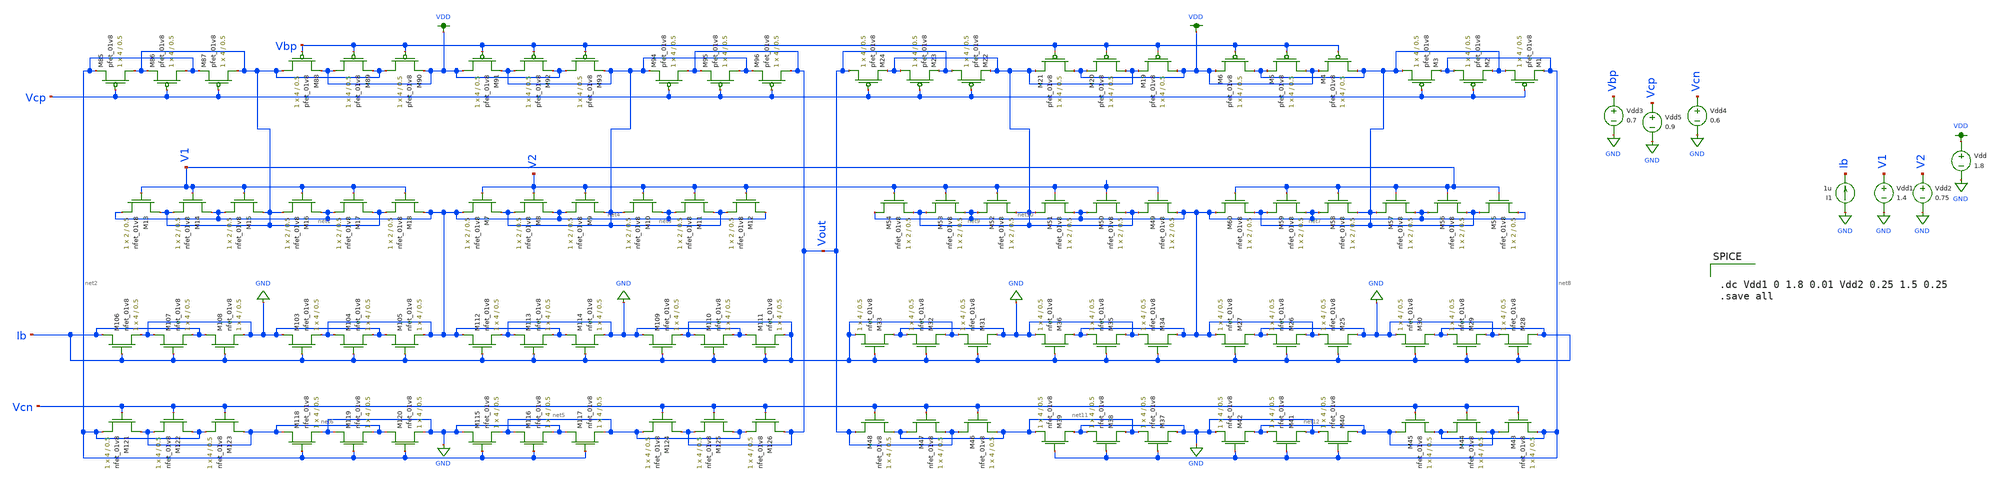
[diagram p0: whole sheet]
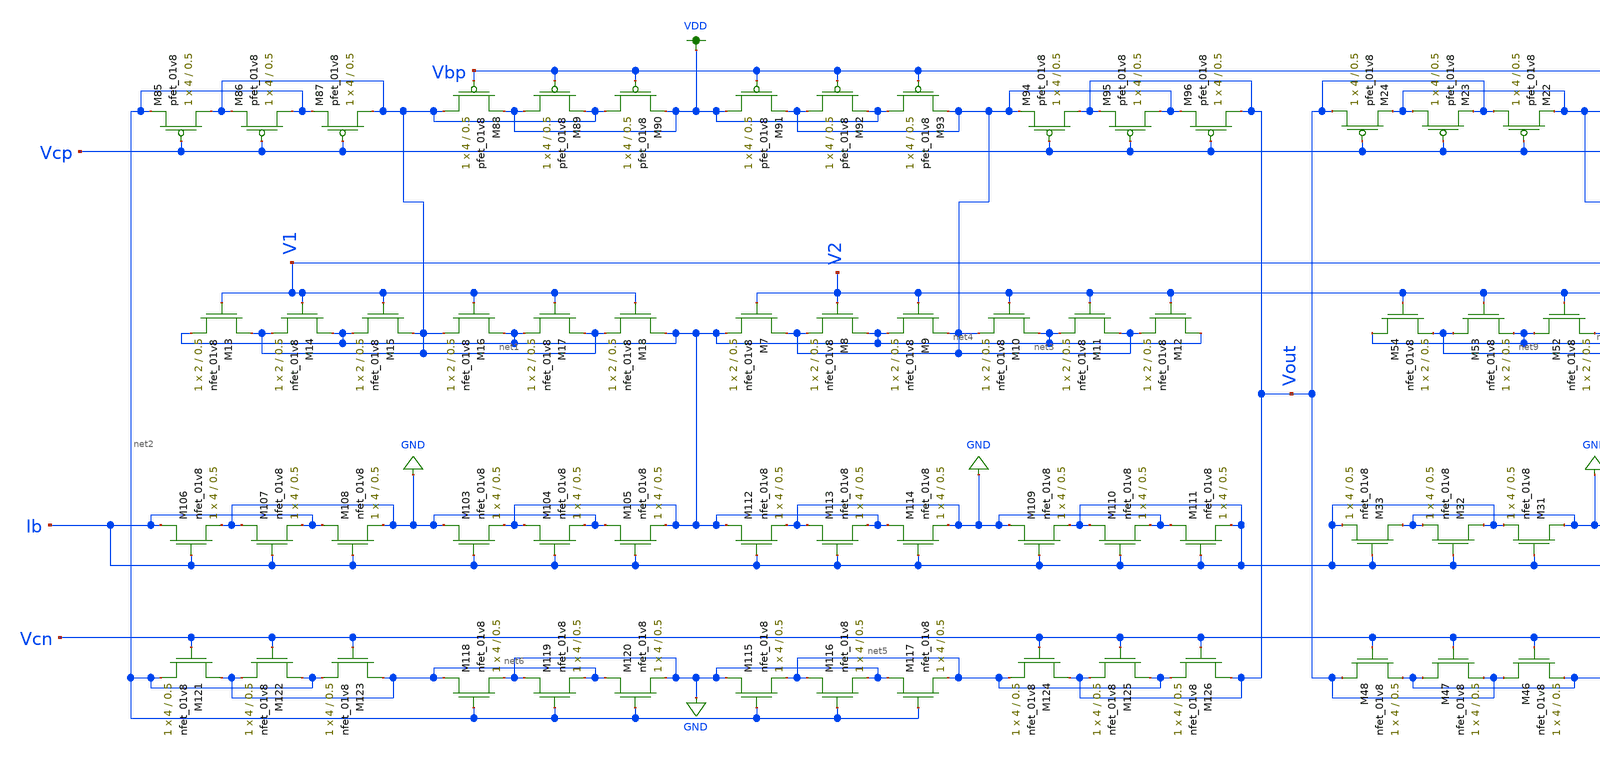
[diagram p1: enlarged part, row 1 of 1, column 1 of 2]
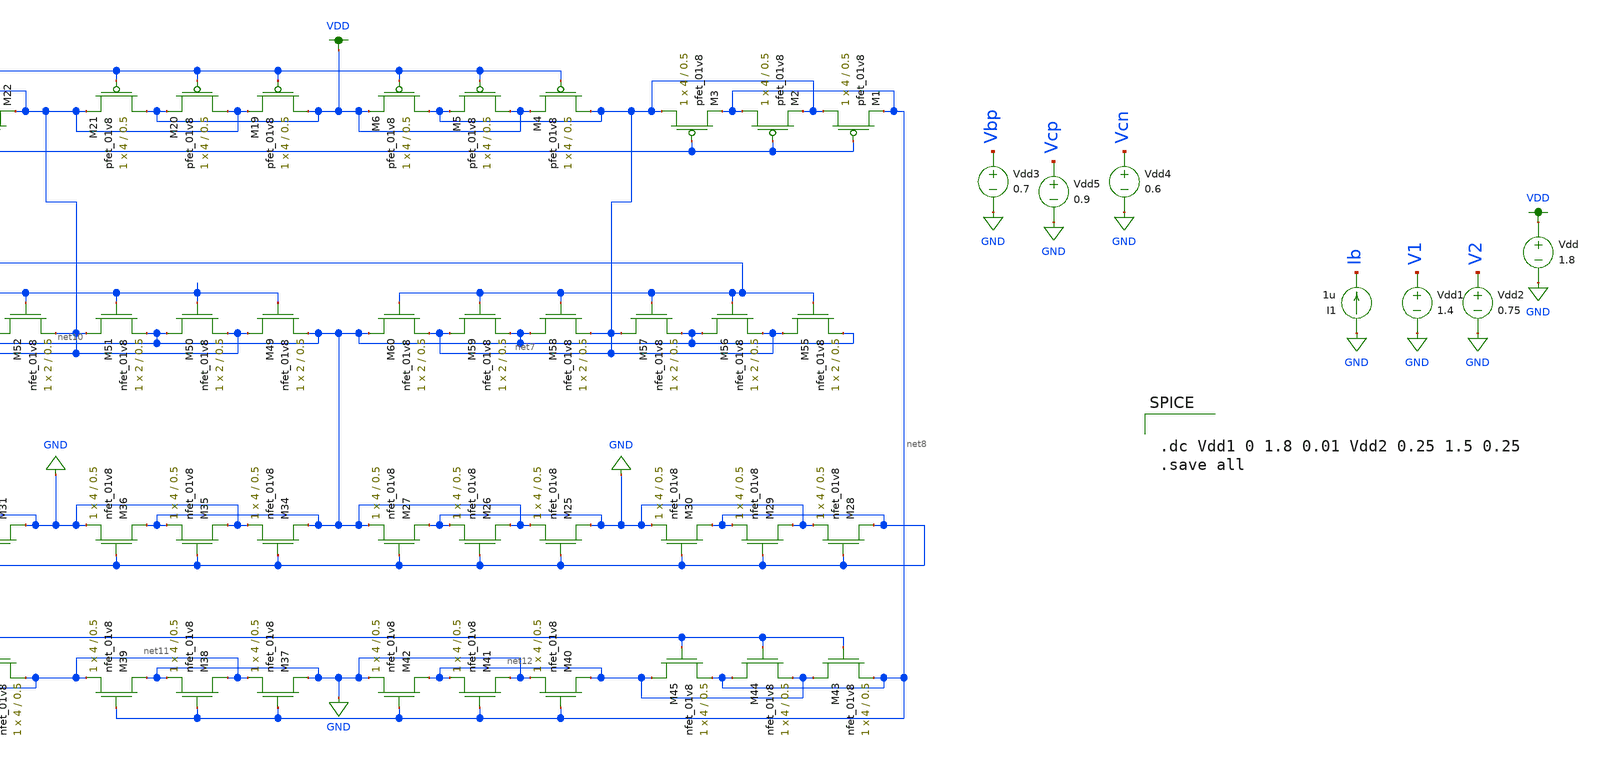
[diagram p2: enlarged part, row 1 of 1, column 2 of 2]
** sch_path: mp3/schematic/amp_lds_tran.sch
**.subckt amp_lds_tran
Vdd1 V1 GND 1.4
Vdd2 V2 GND 0.75
I1 GND Ib 1u
Vdd VDD GND 1.8
XM85 net1 Vcp net2 VDD sky130_fd_pr__pfet_01v8 L=0.5 W=4 nf=1 ad='int((nf+1)/2) * W/nf * 0.29' as='int((nf+2)/2) * W/nf * 0.29'
+ pd='2*int((nf+1)/2) * (W/nf + 0.29)' ps='2*int((nf+2)/2) * (W/nf + 0.29)' nrd='0.29 / W' nrs='0.29 / W'
+ sa=0 sb=0 sd=0 mult=1 m=1
XM86 net2 Vcp net1 VDD sky130_fd_pr__pfet_01v8 L=0.5 W=4 nf=1 ad='int((nf+1)/2) * W/nf * 0.29' as='int((nf+2)/2) * W/nf * 0.29'
+ pd='2*int((nf+1)/2) * (W/nf + 0.29)' ps='2*int((nf+2)/2) * (W/nf + 0.29)' nrd='0.29 / W' nrs='0.29 / W'
+ sa=0 sb=0 sd=0 mult=1 m=1
XM87 net1 Vcp net2 VDD sky130_fd_pr__pfet_01v8 L=0.5 W=4 nf=1 ad='int((nf+1)/2) * W/nf * 0.29' as='int((nf+2)/2) * W/nf * 0.29'
+ pd='2*int((nf+1)/2) * (W/nf + 0.29)' ps='2*int((nf+2)/2) * (W/nf + 0.29)' nrd='0.29 / W' nrs='0.29 / W'
+ sa=0 sb=0 sd=0 mult=1 m=1
XM88 net1 Vbp VDD VDD sky130_fd_pr__pfet_01v8 L=0.5 W=4 nf=1 ad='int((nf+1)/2) * W/nf * 0.29' as='int((nf+2)/2) * W/nf * 0.29'
+ pd='2*int((nf+1)/2) * (W/nf + 0.29)' ps='2*int((nf+2)/2) * (W/nf + 0.29)' nrd='0.29 / W' nrs='0.29 / W'
+ sa=0 sb=0 sd=0 mult=1 m=1
XM89 VDD Vbp net1 VDD sky130_fd_pr__pfet_01v8 L=0.5 W=4 nf=1 ad='int((nf+1)/2) * W/nf * 0.29' as='int((nf+2)/2) * W/nf * 0.29'
+ pd='2*int((nf+1)/2) * (W/nf + 0.29)' ps='2*int((nf+2)/2) * (W/nf + 0.29)' nrd='0.29 / W' nrs='0.29 / W'
+ sa=0 sb=0 sd=0 mult=1 m=1
XM90 net1 Vbp VDD VDD sky130_fd_pr__pfet_01v8 L=0.5 W=4 nf=1 ad='int((nf+1)/2) * W/nf * 0.29' as='int((nf+2)/2) * W/nf * 0.29'
+ pd='2*int((nf+1)/2) * (W/nf + 0.29)' ps='2*int((nf+2)/2) * (W/nf + 0.29)' nrd='0.29 / W' nrs='0.29 / W'
+ sa=0 sb=0 sd=0 mult=1 m=1
XM91 VDD Vbp net3 VDD sky130_fd_pr__pfet_01v8 L=0.5 W=4 nf=1 ad='int((nf+1)/2) * W/nf * 0.29' as='int((nf+2)/2) * W/nf * 0.29'
+ pd='2*int((nf+1)/2) * (W/nf + 0.29)' ps='2*int((nf+2)/2) * (W/nf + 0.29)' nrd='0.29 / W' nrs='0.29 / W'
+ sa=0 sb=0 sd=0 mult=1 m=1
XM92 net3 Vbp VDD VDD sky130_fd_pr__pfet_01v8 L=0.5 W=4 nf=1 ad='int((nf+1)/2) * W/nf * 0.29' as='int((nf+2)/2) * W/nf * 0.29'
+ pd='2*int((nf+1)/2) * (W/nf + 0.29)' ps='2*int((nf+2)/2) * (W/nf + 0.29)' nrd='0.29 / W' nrs='0.29 / W'
+ sa=0 sb=0 sd=0 mult=1 m=1
XM93 VDD Vbp net3 VDD sky130_fd_pr__pfet_01v8 L=0.5 W=4 nf=1 ad='int((nf+1)/2) * W/nf * 0.29' as='int((nf+2)/2) * W/nf * 0.29'
+ pd='2*int((nf+1)/2) * (W/nf + 0.29)' ps='2*int((nf+2)/2) * (W/nf + 0.29)' nrd='0.29 / W' nrs='0.29 / W'
+ sa=0 sb=0 sd=0 mult=1 m=1
XM94 Vout Vcp net3 VDD sky130_fd_pr__pfet_01v8 L=0.5 W=4 nf=1 ad='int((nf+1)/2) * W/nf * 0.29' as='int((nf+2)/2) * W/nf * 0.29'
+ pd='2*int((nf+1)/2) * (W/nf + 0.29)' ps='2*int((nf+2)/2) * (W/nf + 0.29)' nrd='0.29 / W' nrs='0.29 / W'
+ sa=0 sb=0 sd=0 mult=1 m=1
XM95 net3 Vcp Vout VDD sky130_fd_pr__pfet_01v8 L=0.5 W=4 nf=1 ad='int((nf+1)/2) * W/nf * 0.29' as='int((nf+2)/2) * W/nf * 0.29'
+ pd='2*int((nf+1)/2) * (W/nf + 0.29)' ps='2*int((nf+2)/2) * (W/nf + 0.29)' nrd='0.29 / W' nrs='0.29 / W'
+ sa=0 sb=0 sd=0 mult=1 m=1
XM96 Vout Vcp net3 VDD sky130_fd_pr__pfet_01v8 L=0.5 W=4 nf=1 ad='int((nf+1)/2) * W/nf * 0.29' as='int((nf+2)/2) * W/nf * 0.29'
+ pd='2*int((nf+1)/2) * (W/nf + 0.29)' ps='2*int((nf+2)/2) * (W/nf + 0.29)' nrd='0.29 / W' nrs='0.29 / W'
+ sa=0 sb=0 sd=0 mult=1 m=1
XM103 GND Ib net4 GND sky130_fd_pr__nfet_01v8 L=0.5 W=4 nf=1 ad='int((nf+1)/2) * W/nf * 0.29' as='int((nf+2)/2) * W/nf * 0.29'
+ pd='2*int((nf+1)/2) * (W/nf + 0.29)' ps='2*int((nf+2)/2) * (W/nf + 0.29)' nrd='0.29 / W' nrs='0.29 / W'
+ sa=0 sb=0 sd=0 mult=1 m=1
XM104 net4 Ib GND GND sky130_fd_pr__nfet_01v8 L=0.5 W=4 nf=1 ad='int((nf+1)/2) * W/nf * 0.29' as='int((nf+2)/2) * W/nf * 0.29'
+ pd='2*int((nf+1)/2) * (W/nf + 0.29)' ps='2*int((nf+2)/2) * (W/nf + 0.29)' nrd='0.29 / W' nrs='0.29 / W'
+ sa=0 sb=0 sd=0 mult=1 m=1
XM105 GND Ib net4 GND sky130_fd_pr__nfet_01v8 L=0.5 W=4 nf=1 ad='int((nf+1)/2) * W/nf * 0.29' as='int((nf+2)/2) * W/nf * 0.29'
+ pd='2*int((nf+1)/2) * (W/nf + 0.29)' ps='2*int((nf+2)/2) * (W/nf + 0.29)' nrd='0.29 / W' nrs='0.29 / W'
+ sa=0 sb=0 sd=0 mult=1 m=1
XM106 Ib Ib GND GND sky130_fd_pr__nfet_01v8 L=0.5 W=4 nf=1 ad='int((nf+1)/2) * W/nf * 0.29' as='int((nf+2)/2) * W/nf * 0.29'
+ pd='2*int((nf+1)/2) * (W/nf + 0.29)' ps='2*int((nf+2)/2) * (W/nf + 0.29)' nrd='0.29 / W' nrs='0.29 / W'
+ sa=0 sb=0 sd=0 mult=1 m=1
XM107 GND Ib Ib GND sky130_fd_pr__nfet_01v8 L=0.5 W=4 nf=1 ad='int((nf+1)/2) * W/nf * 0.29' as='int((nf+2)/2) * W/nf * 0.29'
+ pd='2*int((nf+1)/2) * (W/nf + 0.29)' ps='2*int((nf+2)/2) * (W/nf + 0.29)' nrd='0.29 / W' nrs='0.29 / W'
+ sa=0 sb=0 sd=0 mult=1 m=1
XM108 Ib Ib GND GND sky130_fd_pr__nfet_01v8 L=0.5 W=4 nf=1 ad='int((nf+1)/2) * W/nf * 0.29' as='int((nf+2)/2) * W/nf * 0.29'
+ pd='2*int((nf+1)/2) * (W/nf + 0.29)' ps='2*int((nf+2)/2) * (W/nf + 0.29)' nrd='0.29 / W' nrs='0.29 / W'
+ sa=0 sb=0 sd=0 mult=1 m=1
XM109 GND Ib Ib GND sky130_fd_pr__nfet_01v8 L=0.5 W=4 nf=1 ad='int((nf+1)/2) * W/nf * 0.29' as='int((nf+2)/2) * W/nf * 0.29'
+ pd='2*int((nf+1)/2) * (W/nf + 0.29)' ps='2*int((nf+2)/2) * (W/nf + 0.29)' nrd='0.29 / W' nrs='0.29 / W'
+ sa=0 sb=0 sd=0 mult=1 m=1
XM110 Ib Ib GND GND sky130_fd_pr__nfet_01v8 L=0.5 W=4 nf=1 ad='int((nf+1)/2) * W/nf * 0.29' as='int((nf+2)/2) * W/nf * 0.29'
+ pd='2*int((nf+1)/2) * (W/nf + 0.29)' ps='2*int((nf+2)/2) * (W/nf + 0.29)' nrd='0.29 / W' nrs='0.29 / W'
+ sa=0 sb=0 sd=0 mult=1 m=1
XM111 GND Ib Ib GND sky130_fd_pr__nfet_01v8 L=0.5 W=4 nf=1 ad='int((nf+1)/2) * W/nf * 0.29' as='int((nf+2)/2) * W/nf * 0.29'
+ pd='2*int((nf+1)/2) * (W/nf + 0.29)' ps='2*int((nf+2)/2) * (W/nf + 0.29)' nrd='0.29 / W' nrs='0.29 / W'
+ sa=0 sb=0 sd=0 mult=1 m=1
XM112 net4 Ib GND GND sky130_fd_pr__nfet_01v8 L=0.5 W=4 nf=1 ad='int((nf+1)/2) * W/nf * 0.29' as='int((nf+2)/2) * W/nf * 0.29'
+ pd='2*int((nf+1)/2) * (W/nf + 0.29)' ps='2*int((nf+2)/2) * (W/nf + 0.29)' nrd='0.29 / W' nrs='0.29 / W'
+ sa=0 sb=0 sd=0 mult=1 m=1
XM113 GND Ib net4 GND sky130_fd_pr__nfet_01v8 L=0.5 W=4 nf=1 ad='int((nf+1)/2) * W/nf * 0.29' as='int((nf+2)/2) * W/nf * 0.29'
+ pd='2*int((nf+1)/2) * (W/nf + 0.29)' ps='2*int((nf+2)/2) * (W/nf + 0.29)' nrd='0.29 / W' nrs='0.29 / W'
+ sa=0 sb=0 sd=0 mult=1 m=1
XM114 net4 Ib GND GND sky130_fd_pr__nfet_01v8 L=0.5 W=4 nf=1 ad='int((nf+1)/2) * W/nf * 0.29' as='int((nf+2)/2) * W/nf * 0.29'
+ pd='2*int((nf+1)/2) * (W/nf + 0.29)' ps='2*int((nf+2)/2) * (W/nf + 0.29)' nrd='0.29 / W' nrs='0.29 / W'
+ sa=0 sb=0 sd=0 mult=1 m=1
XM115 GND net2 net5 GND sky130_fd_pr__nfet_01v8 L=0.5 W=4 nf=1 ad='int((nf+1)/2) * W/nf * 0.29' as='int((nf+2)/2) * W/nf * 0.29'
+ pd='2*int((nf+1)/2) * (W/nf + 0.29)' ps='2*int((nf+2)/2) * (W/nf + 0.29)' nrd='0.29 / W' nrs='0.29 / W'
+ sa=0 sb=0 sd=0 mult=1 m=1
XM116 net5 net2 GND GND sky130_fd_pr__nfet_01v8 L=0.5 W=4 nf=1 ad='int((nf+1)/2) * W/nf * 0.29' as='int((nf+2)/2) * W/nf * 0.29'
+ pd='2*int((nf+1)/2) * (W/nf + 0.29)' ps='2*int((nf+2)/2) * (W/nf + 0.29)' nrd='0.29 / W' nrs='0.29 / W'
+ sa=0 sb=0 sd=0 mult=1 m=1
XM117 GND net2 net5 GND sky130_fd_pr__nfet_01v8 L=0.5 W=4 nf=1 ad='int((nf+1)/2) * W/nf * 0.29' as='int((nf+2)/2) * W/nf * 0.29'
+ pd='2*int((nf+1)/2) * (W/nf + 0.29)' ps='2*int((nf+2)/2) * (W/nf + 0.29)' nrd='0.29 / W' nrs='0.29 / W'
+ sa=0 sb=0 sd=0 mult=1 m=1
XM118 net6 net2 GND GND sky130_fd_pr__nfet_01v8 L=0.5 W=4 nf=1 ad='int((nf+1)/2) * W/nf * 0.29' as='int((nf+2)/2) * W/nf * 0.29'
+ pd='2*int((nf+1)/2) * (W/nf + 0.29)' ps='2*int((nf+2)/2) * (W/nf + 0.29)' nrd='0.29 / W' nrs='0.29 / W'
+ sa=0 sb=0 sd=0 mult=1 m=1
XM119 GND net2 net6 GND sky130_fd_pr__nfet_01v8 L=0.5 W=4 nf=1 ad='int((nf+1)/2) * W/nf * 0.29' as='int((nf+2)/2) * W/nf * 0.29'
+ pd='2*int((nf+1)/2) * (W/nf + 0.29)' ps='2*int((nf+2)/2) * (W/nf + 0.29)' nrd='0.29 / W' nrs='0.29 / W'
+ sa=0 sb=0 sd=0 mult=1 m=1
XM120 net6 net2 GND GND sky130_fd_pr__nfet_01v8 L=0.5 W=4 nf=1 ad='int((nf+1)/2) * W/nf * 0.29' as='int((nf+2)/2) * W/nf * 0.29'
+ pd='2*int((nf+1)/2) * (W/nf + 0.29)' ps='2*int((nf+2)/2) * (W/nf + 0.29)' nrd='0.29 / W' nrs='0.29 / W'
+ sa=0 sb=0 sd=0 mult=1 m=1
XM121 net6 Vcn net2 GND sky130_fd_pr__nfet_01v8 L=0.5 W=4 nf=1 ad='int((nf+1)/2) * W/nf * 0.29' as='int((nf+2)/2) * W/nf * 0.29'
+ pd='2*int((nf+1)/2) * (W/nf + 0.29)' ps='2*int((nf+2)/2) * (W/nf + 0.29)' nrd='0.29 / W' nrs='0.29 / W'
+ sa=0 sb=0 sd=0 mult=1 m=1
XM122 net2 Vcn net6 GND sky130_fd_pr__nfet_01v8 L=0.5 W=4 nf=1 ad='int((nf+1)/2) * W/nf * 0.29' as='int((nf+2)/2) * W/nf * 0.29'
+ pd='2*int((nf+1)/2) * (W/nf + 0.29)' ps='2*int((nf+2)/2) * (W/nf + 0.29)' nrd='0.29 / W' nrs='0.29 / W'
+ sa=0 sb=0 sd=0 mult=1 m=1
XM123 net6 Vcn net2 GND sky130_fd_pr__nfet_01v8 L=0.5 W=4 nf=1 ad='int((nf+1)/2) * W/nf * 0.29' as='int((nf+2)/2) * W/nf * 0.29'
+ pd='2*int((nf+1)/2) * (W/nf + 0.29)' ps='2*int((nf+2)/2) * (W/nf + 0.29)' nrd='0.29 / W' nrs='0.29 / W'
+ sa=0 sb=0 sd=0 mult=1 m=1
XM124 Vout Vcn net5 GND sky130_fd_pr__nfet_01v8 L=0.5 W=4 nf=1 ad='int((nf+1)/2) * W/nf * 0.29' as='int((nf+2)/2) * W/nf * 0.29'
+ pd='2*int((nf+1)/2) * (W/nf + 0.29)' ps='2*int((nf+2)/2) * (W/nf + 0.29)' nrd='0.29 / W' nrs='0.29 / W'
+ sa=0 sb=0 sd=0 mult=1 m=1
XM125 net5 Vcn Vout GND sky130_fd_pr__nfet_01v8 L=0.5 W=4 nf=1 ad='int((nf+1)/2) * W/nf * 0.29' as='int((nf+2)/2) * W/nf * 0.29'
+ pd='2*int((nf+1)/2) * (W/nf + 0.29)' ps='2*int((nf+2)/2) * (W/nf + 0.29)' nrd='0.29 / W' nrs='0.29 / W'
+ sa=0 sb=0 sd=0 mult=1 m=1
XM126 Vout Vcn net5 GND sky130_fd_pr__nfet_01v8 L=0.5 W=4 nf=1 ad='int((nf+1)/2) * W/nf * 0.29' as='int((nf+2)/2) * W/nf * 0.29'
+ pd='2*int((nf+1)/2) * (W/nf + 0.29)' ps='2*int((nf+2)/2) * (W/nf + 0.29)' nrd='0.29 / W' nrs='0.29 / W'
+ sa=0 sb=0 sd=0 mult=1 m=1
XM7 net3 V2 net4 GND sky130_fd_pr__nfet_01v8 L=0.5 W=2 nf=1 ad='int((nf+1)/2) * W/nf * 0.29' as='int((nf+2)/2) * W/nf * 0.29'
+ pd='2*int((nf+1)/2) * (W/nf + 0.29)' ps='2*int((nf+2)/2) * (W/nf + 0.29)' nrd='0.29 / W' nrs='0.29 / W'
+ sa=0 sb=0 sd=0 mult=1 m=1
XM8 net4 V2 net3 GND sky130_fd_pr__nfet_01v8 L=0.5 W=2 nf=1 ad='int((nf+1)/2) * W/nf * 0.29' as='int((nf+2)/2) * W/nf * 0.29'
+ pd='2*int((nf+1)/2) * (W/nf + 0.29)' ps='2*int((nf+2)/2) * (W/nf + 0.29)' nrd='0.29 / W' nrs='0.29 / W'
+ sa=0 sb=0 sd=0 mult=1 m=1
XM9 net3 V2 net4 GND sky130_fd_pr__nfet_01v8 L=0.5 W=2 nf=1 ad='int((nf+1)/2) * W/nf * 0.29' as='int((nf+2)/2) * W/nf * 0.29'
+ pd='2*int((nf+1)/2) * (W/nf + 0.29)' ps='2*int((nf+2)/2) * (W/nf + 0.29)' nrd='0.29 / W' nrs='0.29 / W'
+ sa=0 sb=0 sd=0 mult=1 m=1
XM10 net4 V2 net3 GND sky130_fd_pr__nfet_01v8 L=0.5 W=2 nf=1 ad='int((nf+1)/2) * W/nf * 0.29' as='int((nf+2)/2) * W/nf * 0.29'
+ pd='2*int((nf+1)/2) * (W/nf + 0.29)' ps='2*int((nf+2)/2) * (W/nf + 0.29)' nrd='0.29 / W' nrs='0.29 / W'
+ sa=0 sb=0 sd=0 mult=1 m=1
XM11 net3 V2 net4 GND sky130_fd_pr__nfet_01v8 L=0.5 W=2 nf=1 ad='int((nf+1)/2) * W/nf * 0.29' as='int((nf+2)/2) * W/nf * 0.29'
+ pd='2*int((nf+1)/2) * (W/nf + 0.29)' ps='2*int((nf+2)/2) * (W/nf + 0.29)' nrd='0.29 / W' nrs='0.29 / W'
+ sa=0 sb=0 sd=0 mult=1 m=1
XM12 net4 V2 net3 GND sky130_fd_pr__nfet_01v8 L=0.5 W=2 nf=1 ad='int((nf+1)/2) * W/nf * 0.29' as='int((nf+2)/2) * W/nf * 0.29'
+ pd='2*int((nf+1)/2) * (W/nf + 0.29)' ps='2*int((nf+2)/2) * (W/nf + 0.29)' nrd='0.29 / W' nrs='0.29 / W'
+ sa=0 sb=0 sd=0 mult=1 m=1
XM13 net1 V1 net4 GND sky130_fd_pr__nfet_01v8 L=0.5 W=2 nf=1 ad='int((nf+1)/2) * W/nf * 0.29' as='int((nf+2)/2) * W/nf * 0.29'
+ pd='2*int((nf+1)/2) * (W/nf + 0.29)' ps='2*int((nf+2)/2) * (W/nf + 0.29)' nrd='0.29 / W' nrs='0.29 / W'
+ sa=0 sb=0 sd=0 mult=1 m=1
XM14 net4 V1 net1 GND sky130_fd_pr__nfet_01v8 L=0.5 W=2 nf=1 ad='int((nf+1)/2) * W/nf * 0.29' as='int((nf+2)/2) * W/nf * 0.29'
+ pd='2*int((nf+1)/2) * (W/nf + 0.29)' ps='2*int((nf+2)/2) * (W/nf + 0.29)' nrd='0.29 / W' nrs='0.29 / W'
+ sa=0 sb=0 sd=0 mult=1 m=1
XM15 net1 V1 net4 GND sky130_fd_pr__nfet_01v8 L=0.5 W=2 nf=1 ad='int((nf+1)/2) * W/nf * 0.29' as='int((nf+2)/2) * W/nf * 0.29'
+ pd='2*int((nf+1)/2) * (W/nf + 0.29)' ps='2*int((nf+2)/2) * (W/nf + 0.29)' nrd='0.29 / W' nrs='0.29 / W'
+ sa=0 sb=0 sd=0 mult=1 m=1
XM16 net4 V1 net1 GND sky130_fd_pr__nfet_01v8 L=0.5 W=2 nf=1 ad='int((nf+1)/2) * W/nf * 0.29' as='int((nf+2)/2) * W/nf * 0.29'
+ pd='2*int((nf+1)/2) * (W/nf + 0.29)' ps='2*int((nf+2)/2) * (W/nf + 0.29)' nrd='0.29 / W' nrs='0.29 / W'
+ sa=0 sb=0 sd=0 mult=1 m=1
XM17 net1 V1 net4 GND sky130_fd_pr__nfet_01v8 L=0.5 W=2 nf=1 ad='int((nf+1)/2) * W/nf * 0.29' as='int((nf+2)/2) * W/nf * 0.29'
+ pd='2*int((nf+1)/2) * (W/nf + 0.29)' ps='2*int((nf+2)/2) * (W/nf + 0.29)' nrd='0.29 / W' nrs='0.29 / W'
+ sa=0 sb=0 sd=0 mult=1 m=1
XM18 net4 V1 net1 GND sky130_fd_pr__nfet_01v8 L=0.5 W=2 nf=1 ad='int((nf+1)/2) * W/nf * 0.29' as='int((nf+2)/2) * W/nf * 0.29'
+ pd='2*int((nf+1)/2) * (W/nf + 0.29)' ps='2*int((nf+2)/2) * (W/nf + 0.29)' nrd='0.29 / W' nrs='0.29 / W'
+ sa=0 sb=0 sd=0 mult=1 m=1
XM1 net7 Vcp net8 VDD sky130_fd_pr__pfet_01v8 L=0.5 W=4 nf=1 ad='int((nf+1)/2) * W/nf * 0.29' as='int((nf+2)/2) * W/nf * 0.29'
+ pd='2*int((nf+1)/2) * (W/nf + 0.29)' ps='2*int((nf+2)/2) * (W/nf + 0.29)' nrd='0.29 / W' nrs='0.29 / W'
+ sa=0 sb=0 sd=0 mult=1 m=1
XM2 net8 Vcp net7 VDD sky130_fd_pr__pfet_01v8 L=0.5 W=4 nf=1 ad='int((nf+1)/2) * W/nf * 0.29' as='int((nf+2)/2) * W/nf * 0.29'
+ pd='2*int((nf+1)/2) * (W/nf + 0.29)' ps='2*int((nf+2)/2) * (W/nf + 0.29)' nrd='0.29 / W' nrs='0.29 / W'
+ sa=0 sb=0 sd=0 mult=1 m=1
XM3 net7 Vcp net8 VDD sky130_fd_pr__pfet_01v8 L=0.5 W=4 nf=1 ad='int((nf+1)/2) * W/nf * 0.29' as='int((nf+2)/2) * W/nf * 0.29'
+ pd='2*int((nf+1)/2) * (W/nf + 0.29)' ps='2*int((nf+2)/2) * (W/nf + 0.29)' nrd='0.29 / W' nrs='0.29 / W'
+ sa=0 sb=0 sd=0 mult=1 m=1
XM4 net7 Vbp VDD VDD sky130_fd_pr__pfet_01v8 L=0.5 W=4 nf=1 ad='int((nf+1)/2) * W/nf * 0.29' as='int((nf+2)/2) * W/nf * 0.29'
+ pd='2*int((nf+1)/2) * (W/nf + 0.29)' ps='2*int((nf+2)/2) * (W/nf + 0.29)' nrd='0.29 / W' nrs='0.29 / W'
+ sa=0 sb=0 sd=0 mult=1 m=1
XM5 VDD Vbp net7 VDD sky130_fd_pr__pfet_01v8 L=0.5 W=4 nf=1 ad='int((nf+1)/2) * W/nf * 0.29' as='int((nf+2)/2) * W/nf * 0.29'
+ pd='2*int((nf+1)/2) * (W/nf + 0.29)' ps='2*int((nf+2)/2) * (W/nf + 0.29)' nrd='0.29 / W' nrs='0.29 / W'
+ sa=0 sb=0 sd=0 mult=1 m=1
XM6 net7 Vbp VDD VDD sky130_fd_pr__pfet_01v8 L=0.5 W=4 nf=1 ad='int((nf+1)/2) * W/nf * 0.29' as='int((nf+2)/2) * W/nf * 0.29'
+ pd='2*int((nf+1)/2) * (W/nf + 0.29)' ps='2*int((nf+2)/2) * (W/nf + 0.29)' nrd='0.29 / W' nrs='0.29 / W'
+ sa=0 sb=0 sd=0 mult=1 m=1
XM19 VDD Vbp net9 VDD sky130_fd_pr__pfet_01v8 L=0.5 W=4 nf=1 ad='int((nf+1)/2) * W/nf * 0.29' as='int((nf+2)/2) * W/nf * 0.29'
+ pd='2*int((nf+1)/2) * (W/nf + 0.29)' ps='2*int((nf+2)/2) * (W/nf + 0.29)' nrd='0.29 / W' nrs='0.29 / W'
+ sa=0 sb=0 sd=0 mult=1 m=1
XM20 net9 Vbp VDD VDD sky130_fd_pr__pfet_01v8 L=0.5 W=4 nf=1 ad='int((nf+1)/2) * W/nf * 0.29' as='int((nf+2)/2) * W/nf * 0.29'
+ pd='2*int((nf+1)/2) * (W/nf + 0.29)' ps='2*int((nf+2)/2) * (W/nf + 0.29)' nrd='0.29 / W' nrs='0.29 / W'
+ sa=0 sb=0 sd=0 mult=1 m=1
XM21 VDD Vbp net9 VDD sky130_fd_pr__pfet_01v8 L=0.5 W=4 nf=1 ad='int((nf+1)/2) * W/nf * 0.29' as='int((nf+2)/2) * W/nf * 0.29'
+ pd='2*int((nf+1)/2) * (W/nf + 0.29)' ps='2*int((nf+2)/2) * (W/nf + 0.29)' nrd='0.29 / W' nrs='0.29 / W'
+ sa=0 sb=0 sd=0 mult=1 m=1
XM22 Vout Vcp net9 VDD sky130_fd_pr__pfet_01v8 L=0.5 W=4 nf=1 ad='int((nf+1)/2) * W/nf * 0.29' as='int((nf+2)/2) * W/nf * 0.29'
+ pd='2*int((nf+1)/2) * (W/nf + 0.29)' ps='2*int((nf+2)/2) * (W/nf + 0.29)' nrd='0.29 / W' nrs='0.29 / W'
+ sa=0 sb=0 sd=0 mult=1 m=1
XM23 net9 Vcp Vout VDD sky130_fd_pr__pfet_01v8 L=0.5 W=4 nf=1 ad='int((nf+1)/2) * W/nf * 0.29' as='int((nf+2)/2) * W/nf * 0.29'
+ pd='2*int((nf+1)/2) * (W/nf + 0.29)' ps='2*int((nf+2)/2) * (W/nf + 0.29)' nrd='0.29 / W' nrs='0.29 / W'
+ sa=0 sb=0 sd=0 mult=1 m=1
XM24 Vout Vcp net9 VDD sky130_fd_pr__pfet_01v8 L=0.5 W=4 nf=1 ad='int((nf+1)/2) * W/nf * 0.29' as='int((nf+2)/2) * W/nf * 0.29'
+ pd='2*int((nf+1)/2) * (W/nf + 0.29)' ps='2*int((nf+2)/2) * (W/nf + 0.29)' nrd='0.29 / W' nrs='0.29 / W'
+ sa=0 sb=0 sd=0 mult=1 m=1
XM25 GND Ib net10 GND sky130_fd_pr__nfet_01v8 L=0.5 W=4 nf=1 ad='int((nf+1)/2) * W/nf * 0.29' as='int((nf+2)/2) * W/nf * 0.29'
+ pd='2*int((nf+1)/2) * (W/nf + 0.29)' ps='2*int((nf+2)/2) * (W/nf + 0.29)' nrd='0.29 / W' nrs='0.29 / W'
+ sa=0 sb=0 sd=0 mult=1 m=1
XM26 net10 Ib GND GND sky130_fd_pr__nfet_01v8 L=0.5 W=4 nf=1 ad='int((nf+1)/2) * W/nf * 0.29' as='int((nf+2)/2) * W/nf * 0.29'
+ pd='2*int((nf+1)/2) * (W/nf + 0.29)' ps='2*int((nf+2)/2) * (W/nf + 0.29)' nrd='0.29 / W' nrs='0.29 / W'
+ sa=0 sb=0 sd=0 mult=1 m=1
XM27 GND Ib net10 GND sky130_fd_pr__nfet_01v8 L=0.5 W=4 nf=1 ad='int((nf+1)/2) * W/nf * 0.29' as='int((nf+2)/2) * W/nf * 0.29'
+ pd='2*int((nf+1)/2) * (W/nf + 0.29)' ps='2*int((nf+2)/2) * (W/nf + 0.29)' nrd='0.29 / W' nrs='0.29 / W'
+ sa=0 sb=0 sd=0 mult=1 m=1
XM28 Ib Ib GND GND sky130_fd_pr__nfet_01v8 L=0.5 W=4 nf=1 ad='int((nf+1)/2) * W/nf * 0.29' as='int((nf+2)/2) * W/nf * 0.29'
+ pd='2*int((nf+1)/2) * (W/nf + 0.29)' ps='2*int((nf+2)/2) * (W/nf + 0.29)' nrd='0.29 / W' nrs='0.29 / W'
+ sa=0 sb=0 sd=0 mult=1 m=1
XM29 GND Ib Ib GND sky130_fd_pr__nfet_01v8 L=0.5 W=4 nf=1 ad='int((nf+1)/2) * W/nf * 0.29' as='int((nf+2)/2) * W/nf * 0.29'
+ pd='2*int((nf+1)/2) * (W/nf + 0.29)' ps='2*int((nf+2)/2) * (W/nf + 0.29)' nrd='0.29 / W' nrs='0.29 / W'
+ sa=0 sb=0 sd=0 mult=1 m=1
XM30 Ib Ib GND GND sky130_fd_pr__nfet_01v8 L=0.5 W=4 nf=1 ad='int((nf+1)/2) * W/nf * 0.29' as='int((nf+2)/2) * W/nf * 0.29'
+ pd='2*int((nf+1)/2) * (W/nf + 0.29)' ps='2*int((nf+2)/2) * (W/nf + 0.29)' nrd='0.29 / W' nrs='0.29 / W'
+ sa=0 sb=0 sd=0 mult=1 m=1
XM31 GND Ib Ib GND sky130_fd_pr__nfet_01v8 L=0.5 W=4 nf=1 ad='int((nf+1)/2) * W/nf * 0.29' as='int((nf+2)/2) * W/nf * 0.29'
+ pd='2*int((nf+1)/2) * (W/nf + 0.29)' ps='2*int((nf+2)/2) * (W/nf + 0.29)' nrd='0.29 / W' nrs='0.29 / W'
+ sa=0 sb=0 sd=0 mult=1 m=1
XM32 Ib Ib GND GND sky130_fd_pr__nfet_01v8 L=0.5 W=4 nf=1 ad='int((nf+1)/2) * W/nf * 0.29' as='int((nf+2)/2) * W/nf * 0.29'
+ pd='2*int((nf+1)/2) * (W/nf + 0.29)' ps='2*int((nf+2)/2) * (W/nf + 0.29)' nrd='0.29 / W' nrs='0.29 / W'
+ sa=0 sb=0 sd=0 mult=1 m=1
XM33 GND Ib Ib GND sky130_fd_pr__nfet_01v8 L=0.5 W=4 nf=1 ad='int((nf+1)/2) * W/nf * 0.29' as='int((nf+2)/2) * W/nf * 0.29'
+ pd='2*int((nf+1)/2) * (W/nf + 0.29)' ps='2*int((nf+2)/2) * (W/nf + 0.29)' nrd='0.29 / W' nrs='0.29 / W'
+ sa=0 sb=0 sd=0 mult=1 m=1
XM34 net10 Ib GND GND sky130_fd_pr__nfet_01v8 L=0.5 W=4 nf=1 ad='int((nf+1)/2) * W/nf * 0.29' as='int((nf+2)/2) * W/nf * 0.29'
+ pd='2*int((nf+1)/2) * (W/nf + 0.29)' ps='2*int((nf+2)/2) * (W/nf + 0.29)' nrd='0.29 / W' nrs='0.29 / W'
+ sa=0 sb=0 sd=0 mult=1 m=1
XM35 GND Ib net10 GND sky130_fd_pr__nfet_01v8 L=0.5 W=4 nf=1 ad='int((nf+1)/2) * W/nf * 0.29' as='int((nf+2)/2) * W/nf * 0.29'
+ pd='2*int((nf+1)/2) * (W/nf + 0.29)' ps='2*int((nf+2)/2) * (W/nf + 0.29)' nrd='0.29 / W' nrs='0.29 / W'
+ sa=0 sb=0 sd=0 mult=1 m=1
XM36 net10 Ib GND GND sky130_fd_pr__nfet_01v8 L=0.5 W=4 nf=1 ad='int((nf+1)/2) * W/nf * 0.29' as='int((nf+2)/2) * W/nf * 0.29'
+ pd='2*int((nf+1)/2) * (W/nf + 0.29)' ps='2*int((nf+2)/2) * (W/nf + 0.29)' nrd='0.29 / W' nrs='0.29 / W'
+ sa=0 sb=0 sd=0 mult=1 m=1
XM37 GND net8 net11 GND sky130_fd_pr__nfet_01v8 L=0.5 W=4 nf=1 ad='int((nf+1)/2) * W/nf * 0.29' as='int((nf+2)/2) * W/nf * 0.29'
+ pd='2*int((nf+1)/2) * (W/nf + 0.29)' ps='2*int((nf+2)/2) * (W/nf + 0.29)' nrd='0.29 / W' nrs='0.29 / W'
+ sa=0 sb=0 sd=0 mult=1 m=1
XM38 net11 net8 GND GND sky130_fd_pr__nfet_01v8 L=0.5 W=4 nf=1 ad='int((nf+1)/2) * W/nf * 0.29' as='int((nf+2)/2) * W/nf * 0.29'
+ pd='2*int((nf+1)/2) * (W/nf + 0.29)' ps='2*int((nf+2)/2) * (W/nf + 0.29)' nrd='0.29 / W' nrs='0.29 / W'
+ sa=0 sb=0 sd=0 mult=1 m=1
XM39 GND net8 net11 GND sky130_fd_pr__nfet_01v8 L=0.5 W=4 nf=1 ad='int((nf+1)/2) * W/nf * 0.29' as='int((nf+2)/2) * W/nf * 0.29'
+ pd='2*int((nf+1)/2) * (W/nf + 0.29)' ps='2*int((nf+2)/2) * (W/nf + 0.29)' nrd='0.29 / W' nrs='0.29 / W'
+ sa=0 sb=0 sd=0 mult=1 m=1
XM40 net12 net8 GND GND sky130_fd_pr__nfet_01v8 L=0.5 W=4 nf=1 ad='int((nf+1)/2) * W/nf * 0.29' as='int((nf+2)/2) * W/nf * 0.29'
+ pd='2*int((nf+1)/2) * (W/nf + 0.29)' ps='2*int((nf+2)/2) * (W/nf + 0.29)' nrd='0.29 / W' nrs='0.29 / W'
+ sa=0 sb=0 sd=0 mult=1 m=1
XM41 GND net8 net12 GND sky130_fd_pr__nfet_01v8 L=0.5 W=4 nf=1 ad='int((nf+1)/2) * W/nf * 0.29' as='int((nf+2)/2) * W/nf * 0.29'
+ pd='2*int((nf+1)/2) * (W/nf + 0.29)' ps='2*int((nf+2)/2) * (W/nf + 0.29)' nrd='0.29 / W' nrs='0.29 / W'
+ sa=0 sb=0 sd=0 mult=1 m=1
XM42 net12 net8 GND GND sky130_fd_pr__nfet_01v8 L=0.5 W=4 nf=1 ad='int((nf+1)/2) * W/nf * 0.29' as='int((nf+2)/2) * W/nf * 0.29'
+ pd='2*int((nf+1)/2) * (W/nf + 0.29)' ps='2*int((nf+2)/2) * (W/nf + 0.29)' nrd='0.29 / W' nrs='0.29 / W'
+ sa=0 sb=0 sd=0 mult=1 m=1
XM43 net12 Vcn net8 GND sky130_fd_pr__nfet_01v8 L=0.5 W=4 nf=1 ad='int((nf+1)/2) * W/nf * 0.29' as='int((nf+2)/2) * W/nf * 0.29'
+ pd='2*int((nf+1)/2) * (W/nf + 0.29)' ps='2*int((nf+2)/2) * (W/nf + 0.29)' nrd='0.29 / W' nrs='0.29 / W'
+ sa=0 sb=0 sd=0 mult=1 m=1
XM44 net8 Vcn net12 GND sky130_fd_pr__nfet_01v8 L=0.5 W=4 nf=1 ad='int((nf+1)/2) * W/nf * 0.29' as='int((nf+2)/2) * W/nf * 0.29'
+ pd='2*int((nf+1)/2) * (W/nf + 0.29)' ps='2*int((nf+2)/2) * (W/nf + 0.29)' nrd='0.29 / W' nrs='0.29 / W'
+ sa=0 sb=0 sd=0 mult=1 m=1
XM45 net12 Vcn net8 GND sky130_fd_pr__nfet_01v8 L=0.5 W=4 nf=1 ad='int((nf+1)/2) * W/nf * 0.29' as='int((nf+2)/2) * W/nf * 0.29'
+ pd='2*int((nf+1)/2) * (W/nf + 0.29)' ps='2*int((nf+2)/2) * (W/nf + 0.29)' nrd='0.29 / W' nrs='0.29 / W'
+ sa=0 sb=0 sd=0 mult=1 m=1
XM46 Vout Vcn net11 GND sky130_fd_pr__nfet_01v8 L=0.5 W=4 nf=1 ad='int((nf+1)/2) * W/nf * 0.29' as='int((nf+2)/2) * W/nf * 0.29'
+ pd='2*int((nf+1)/2) * (W/nf + 0.29)' ps='2*int((nf+2)/2) * (W/nf + 0.29)' nrd='0.29 / W' nrs='0.29 / W'
+ sa=0 sb=0 sd=0 mult=1 m=1
XM47 net11 Vcn Vout GND sky130_fd_pr__nfet_01v8 L=0.5 W=4 nf=1 ad='int((nf+1)/2) * W/nf * 0.29' as='int((nf+2)/2) * W/nf * 0.29'
+ pd='2*int((nf+1)/2) * (W/nf + 0.29)' ps='2*int((nf+2)/2) * (W/nf + 0.29)' nrd='0.29 / W' nrs='0.29 / W'
+ sa=0 sb=0 sd=0 mult=1 m=1
XM48 Vout Vcn net11 GND sky130_fd_pr__nfet_01v8 L=0.5 W=4 nf=1 ad='int((nf+1)/2) * W/nf * 0.29' as='int((nf+2)/2) * W/nf * 0.29'
+ pd='2*int((nf+1)/2) * (W/nf + 0.29)' ps='2*int((nf+2)/2) * (W/nf + 0.29)' nrd='0.29 / W' nrs='0.29 / W'
+ sa=0 sb=0 sd=0 mult=1 m=1
XM49 net9 V2 net10 GND sky130_fd_pr__nfet_01v8 L=0.5 W=2 nf=1 ad='int((nf+1)/2) * W/nf * 0.29' as='int((nf+2)/2) * W/nf * 0.29'
+ pd='2*int((nf+1)/2) * (W/nf + 0.29)' ps='2*int((nf+2)/2) * (W/nf + 0.29)' nrd='0.29 / W' nrs='0.29 / W'
+ sa=0 sb=0 sd=0 mult=1 m=1
XM50 net10 V2 net9 GND sky130_fd_pr__nfet_01v8 L=0.5 W=2 nf=1 ad='int((nf+1)/2) * W/nf * 0.29' as='int((nf+2)/2) * W/nf * 0.29'
+ pd='2*int((nf+1)/2) * (W/nf + 0.29)' ps='2*int((nf+2)/2) * (W/nf + 0.29)' nrd='0.29 / W' nrs='0.29 / W'
+ sa=0 sb=0 sd=0 mult=1 m=1
XM51 net9 V2 net10 GND sky130_fd_pr__nfet_01v8 L=0.5 W=2 nf=1 ad='int((nf+1)/2) * W/nf * 0.29' as='int((nf+2)/2) * W/nf * 0.29'
+ pd='2*int((nf+1)/2) * (W/nf + 0.29)' ps='2*int((nf+2)/2) * (W/nf + 0.29)' nrd='0.29 / W' nrs='0.29 / W'
+ sa=0 sb=0 sd=0 mult=1 m=1
XM52 net10 V2 net9 GND sky130_fd_pr__nfet_01v8 L=0.5 W=2 nf=1 ad='int((nf+1)/2) * W/nf * 0.29' as='int((nf+2)/2) * W/nf * 0.29'
+ pd='2*int((nf+1)/2) * (W/nf + 0.29)' ps='2*int((nf+2)/2) * (W/nf + 0.29)' nrd='0.29 / W' nrs='0.29 / W'
+ sa=0 sb=0 sd=0 mult=1 m=1
XM53 net9 V2 net10 GND sky130_fd_pr__nfet_01v8 L=0.5 W=2 nf=1 ad='int((nf+1)/2) * W/nf * 0.29' as='int((nf+2)/2) * W/nf * 0.29'
+ pd='2*int((nf+1)/2) * (W/nf + 0.29)' ps='2*int((nf+2)/2) * (W/nf + 0.29)' nrd='0.29 / W' nrs='0.29 / W'
+ sa=0 sb=0 sd=0 mult=1 m=1
XM54 net10 V2 net9 GND sky130_fd_pr__nfet_01v8 L=0.5 W=2 nf=1 ad='int((nf+1)/2) * W/nf * 0.29' as='int((nf+2)/2) * W/nf * 0.29'
+ pd='2*int((nf+1)/2) * (W/nf + 0.29)' ps='2*int((nf+2)/2) * (W/nf + 0.29)' nrd='0.29 / W' nrs='0.29 / W'
+ sa=0 sb=0 sd=0 mult=1 m=1
XM55 net7 V1 net10 GND sky130_fd_pr__nfet_01v8 L=0.5 W=2 nf=1 ad='int((nf+1)/2) * W/nf * 0.29' as='int((nf+2)/2) * W/nf * 0.29'
+ pd='2*int((nf+1)/2) * (W/nf + 0.29)' ps='2*int((nf+2)/2) * (W/nf + 0.29)' nrd='0.29 / W' nrs='0.29 / W'
+ sa=0 sb=0 sd=0 mult=1 m=1
XM56 net10 V1 net7 GND sky130_fd_pr__nfet_01v8 L=0.5 W=2 nf=1 ad='int((nf+1)/2) * W/nf * 0.29' as='int((nf+2)/2) * W/nf * 0.29'
+ pd='2*int((nf+1)/2) * (W/nf + 0.29)' ps='2*int((nf+2)/2) * (W/nf + 0.29)' nrd='0.29 / W' nrs='0.29 / W'
+ sa=0 sb=0 sd=0 mult=1 m=1
XM57 net7 V1 net10 GND sky130_fd_pr__nfet_01v8 L=0.5 W=2 nf=1 ad='int((nf+1)/2) * W/nf * 0.29' as='int((nf+2)/2) * W/nf * 0.29'
+ pd='2*int((nf+1)/2) * (W/nf + 0.29)' ps='2*int((nf+2)/2) * (W/nf + 0.29)' nrd='0.29 / W' nrs='0.29 / W'
+ sa=0 sb=0 sd=0 mult=1 m=1
XM58 net10 V1 net7 GND sky130_fd_pr__nfet_01v8 L=0.5 W=2 nf=1 ad='int((nf+1)/2) * W/nf * 0.29' as='int((nf+2)/2) * W/nf * 0.29'
+ pd='2*int((nf+1)/2) * (W/nf + 0.29)' ps='2*int((nf+2)/2) * (W/nf + 0.29)' nrd='0.29 / W' nrs='0.29 / W'
+ sa=0 sb=0 sd=0 mult=1 m=1
XM59 net7 V1 net10 GND sky130_fd_pr__nfet_01v8 L=0.5 W=2 nf=1 ad='int((nf+1)/2) * W/nf * 0.29' as='int((nf+2)/2) * W/nf * 0.29'
+ pd='2*int((nf+1)/2) * (W/nf + 0.29)' ps='2*int((nf+2)/2) * (W/nf + 0.29)' nrd='0.29 / W' nrs='0.29 / W'
+ sa=0 sb=0 sd=0 mult=1 m=1
XM60 net10 V1 net7 GND sky130_fd_pr__nfet_01v8 L=0.5 W=2 nf=1 ad='int((nf+1)/2) * W/nf * 0.29' as='int((nf+2)/2) * W/nf * 0.29'
+ pd='2*int((nf+1)/2) * (W/nf + 0.29)' ps='2*int((nf+2)/2) * (W/nf + 0.29)' nrd='0.29 / W' nrs='0.29 / W'
+ sa=0 sb=0 sd=0 mult=1 m=1
Vdd3 Vbp GND 0.7
Vdd4 Vcn GND 0.6
Vdd5 Vcp GND 0.9
**** begin user architecture code

.option wnflag=1
.lib ~/skywater/skywater-pdk/libraries/sky130_fd_pr_ngspice/latest/models/sky130.lib.spice tt



.dc Vdd1 0 1.8 0.01 Vdd2 0.25 1.5 0.25
.save all

**** end user architecture code
**.ends
.GLOBAL GND
.GLOBAL VDD
.end
